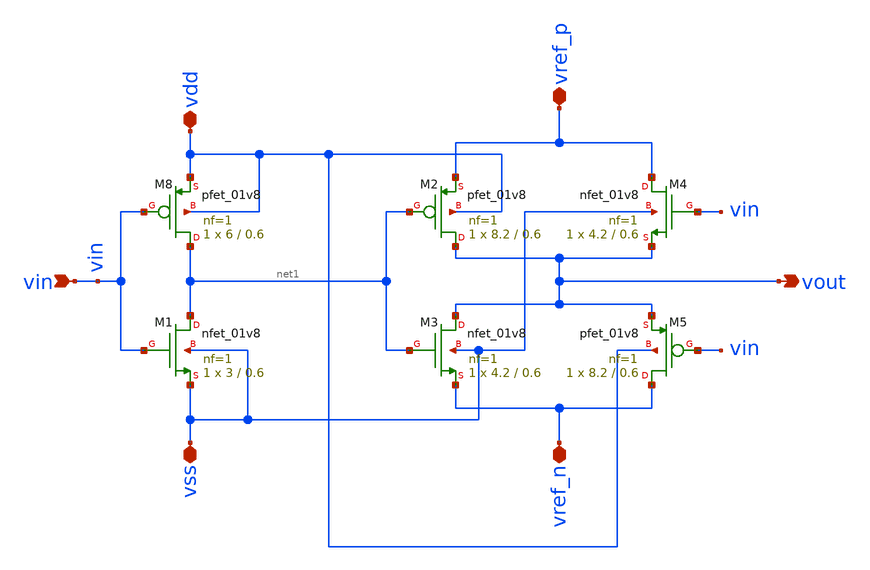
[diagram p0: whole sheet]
** sch_path: xschem/OneBitDAC.sch
**.subckt OneBitDAC vdd vss vin vref_p vref_n vout
*.iopin vdd
*.iopin vss
*.ipin vin
*.iopin vref_p
*.iopin vref_n
*.opin vout
XM8 net1 vin vdd vdd sky130_fd_pr__pfet_01v8 L=0.6 W=6 nf=1 ad='W * 0.29' as='W * 0.29' pd='2 * (W + 0.29)'
+ ps='2 * (W + 0.29)' nrd='0.29 / W' nrs='0.29 / W' sa=0 sb=0 sd=0 mult=1 m=1
XM1 net1 vin vss vss sky130_fd_pr__nfet_01v8 L=0.6 W=3 nf=1 ad='int((nf+1)/2) * W/nf * 0.29' as='int((nf+2)/2) * W/nf * 0.29'
+ pd='2*int((nf+1)/2) * (W/nf + 0.29)' ps='2*int((nf+2)/2) * (W/nf + 0.29)' nrd='0.29 / W' nrs='0.29 / W'
+ sa=0 sb=0 sd=0 mult=1 m=1
XM2 vout net1 vref_p vdd sky130_fd_pr__pfet_01v8 L=0.6 W=8.2 nf=1 ad='int((nf+1)/2) * W/nf * 0.29' as='int((nf+2)/2) * W/nf * 0.29'
+ pd='2*int((nf+1)/2) * (W/nf + 0.29)' ps='2*int((nf+2)/2) * (W/nf + 0.29)' nrd='0.29 / W' nrs='0.29 / W'
+ sa=0 sb=0 sd=0 mult=1 m=1
XM3 vout net1 vref_n vss sky130_fd_pr__nfet_01v8 L=0.6 W=4.2 nf=1 ad='int((nf+1)/2) * W/nf * 0.29' as='int((nf+2)/2) * W/nf * 0.29'
+ pd='2*int((nf+1)/2) * (W/nf + 0.29)' ps='2*int((nf+2)/2) * (W/nf + 0.29)' nrd='0.29 / W' nrs='0.29 / W'
+ sa=0 sb=0 sd=0 mult=1 m=1
XM4 vref_p vin vout vss sky130_fd_pr__nfet_01v8 L=0.6 W=4.2 nf=1 ad='int((nf+1)/2) * W/nf * 0.29' as='int((nf+2)/2) * W/nf * 0.29'
+ pd='2*int((nf+1)/2) * (W/nf + 0.29)' ps='2*int((nf+2)/2) * (W/nf + 0.29)' nrd='0.29 / W' nrs='0.29 / W'
+ sa=0 sb=0 sd=0 mult=1 m=1
XM5 vref_n vin vout vdd sky130_fd_pr__pfet_01v8 L=0.6 W=8.2 nf=1 ad='int((nf+1)/2) * W/nf * 0.29' as='int((nf+2)/2) * W/nf * 0.29'
+ pd='2*int((nf+1)/2) * (W/nf + 0.29)' ps='2*int((nf+2)/2) * (W/nf + 0.29)' nrd='0.29 / W' nrs='0.29 / W'
+ sa=0 sb=0 sd=0 mult=1 m=1
**.ends
.end
